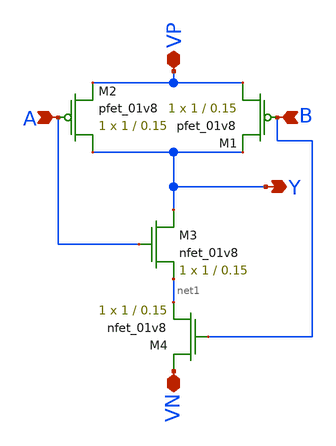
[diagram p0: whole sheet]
** sch_path: Miniproject1/NAND.sch
**.subckt NAND Y A B VP VN
*.opin Y
*.ipin A
*.ipin B
*.iopin VP
*.iopin VN
XM1 VP B Y VDD sky130_fd_pr__pfet_01v8 L=0.15 W=1 nf=1 ad='int((nf+1)/2) * W/nf * 0.29' as='int((nf+2)/2) * W/nf * 0.29'
+ pd='2*int((nf+1)/2) * (W/nf + 0.29)' ps='2*int((nf+2)/2) * (W/nf + 0.29)' nrd='0.29 / W' nrs='0.29 / W'
+ sa=0 sb=0 sd=0 mult=1 m=1
XM2 Y A VP VDD sky130_fd_pr__pfet_01v8 L=0.15 W=1 nf=1 ad='int((nf+1)/2) * W/nf * 0.29' as='int((nf+2)/2) * W/nf * 0.29'
+ pd='2*int((nf+1)/2) * (W/nf + 0.29)' ps='2*int((nf+2)/2) * (W/nf + 0.29)' nrd='0.29 / W' nrs='0.29 / W'
+ sa=0 sb=0 sd=0 mult=1 m=1
XM3 Y A net1 GND sky130_fd_pr__nfet_01v8 L=0.15 W=1 nf=1 ad='int((nf+1)/2) * W/nf * 0.29' as='int((nf+2)/2) * W/nf * 0.29'
+ pd='2*int((nf+1)/2) * (W/nf + 0.29)' ps='2*int((nf+2)/2) * (W/nf + 0.29)' nrd='0.29 / W' nrs='0.29 / W'
+ sa=0 sb=0 sd=0 mult=1 m=1
XM4 VN B net1 GND sky130_fd_pr__nfet_01v8 L=0.15 W=1 nf=1 ad='int((nf+1)/2) * W/nf * 0.29' as='int((nf+2)/2) * W/nf * 0.29'
+ pd='2*int((nf+1)/2) * (W/nf + 0.29)' ps='2*int((nf+2)/2) * (W/nf + 0.29)' nrd='0.29 / W' nrs='0.29 / W'
+ sa=0 sb=0 sd=0 mult=1 m=1
**.ends
.end
